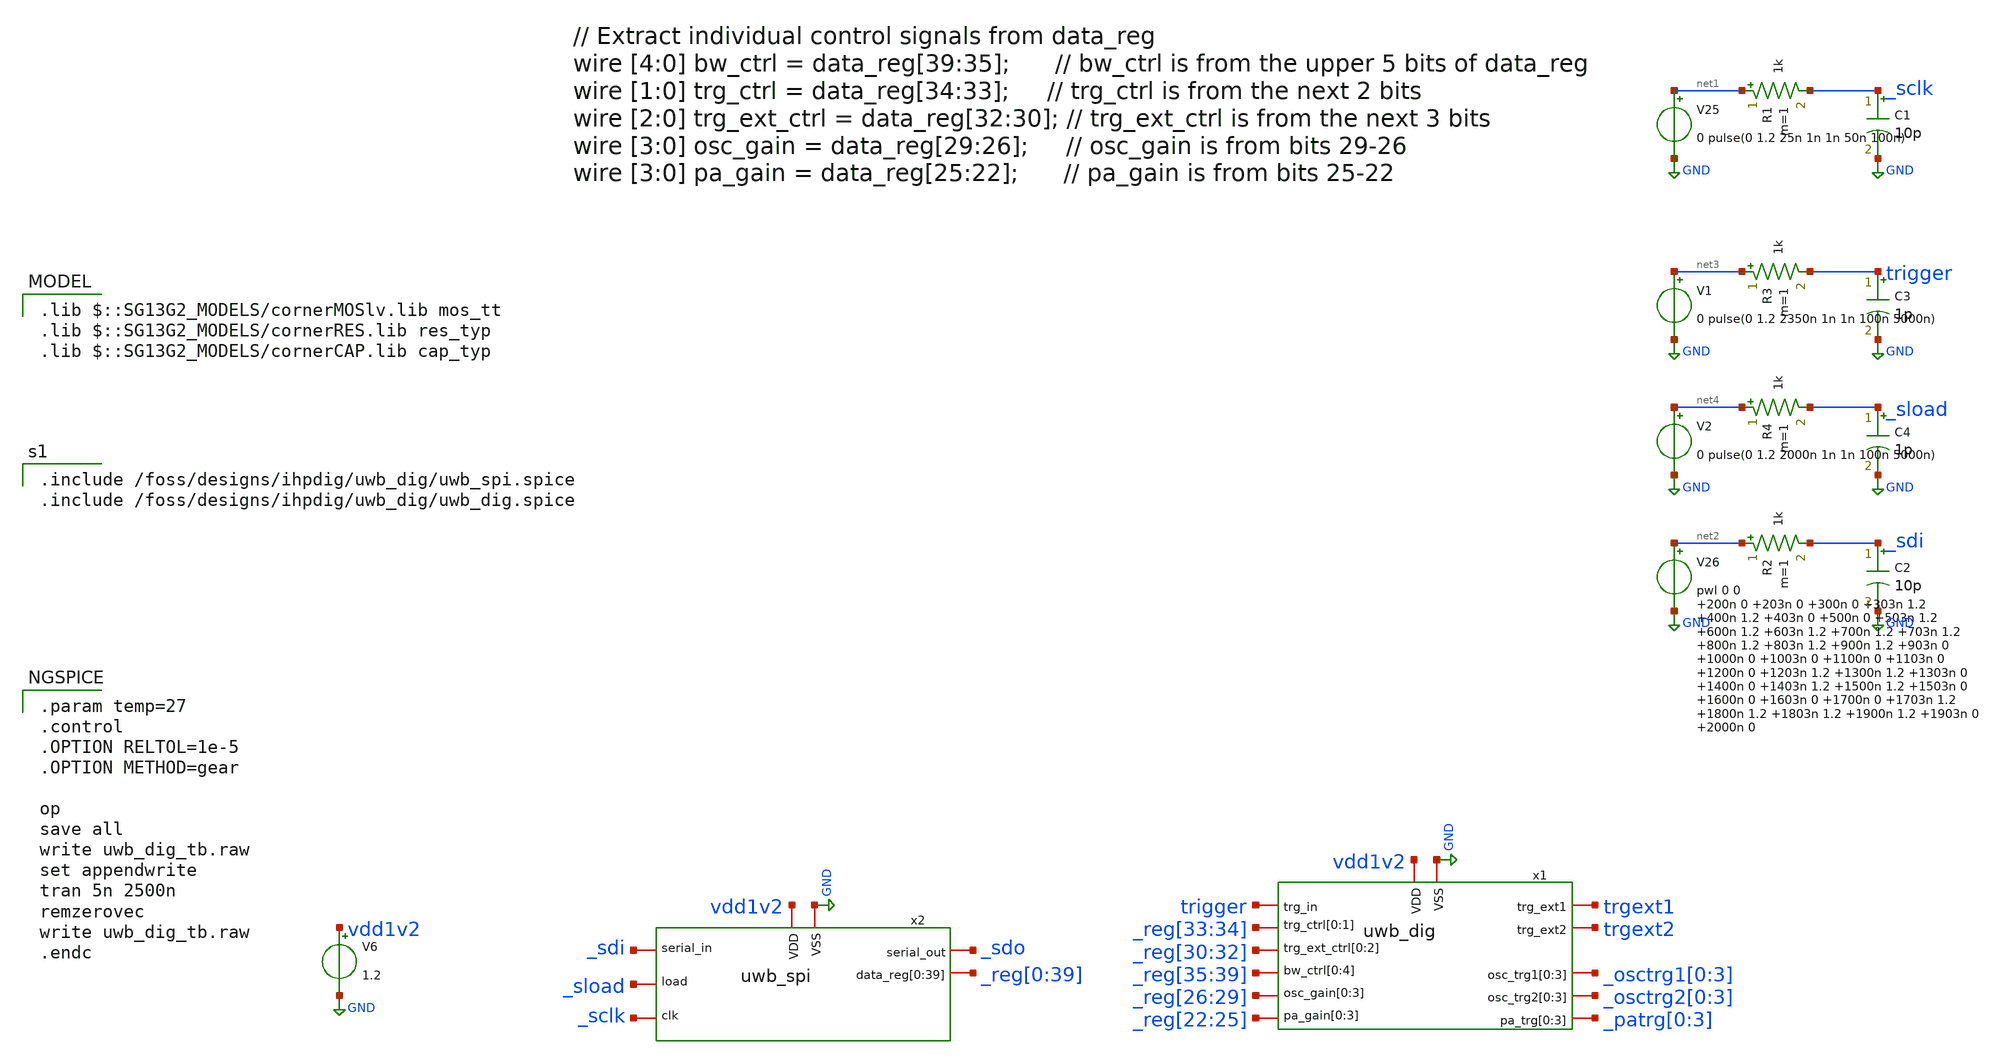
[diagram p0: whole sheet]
** sch_path: JKU_TC2/design_data/xschem/uwb_dig_tb.sch
**.subckt uwb_dig_tb
V6 vdd1v2 GND 1.2
V25 net1 GND 0 pulse(0 1.2 25n 1n 1n 50n 100n)

V26 net2 GND pwl 0 0 200n 0 +203n 0 +300n 0 +303n 1.2 400n 1.2 +403n 0 +500n 0 +503n 1.2 600n 1.2
+ +603n 1.2 +700n 1.2 +703n 1.2 800n 1.2 +803n 1.2 +900n 1.2 +903n 0 1000n 0 +1003n 0 +1100n 0 +1103n 0
+ 1200n 0 +1203n 1.2 +1300n 1.2 +1303n 0 1400n 0 +1403n 1.2 +1500n 1.2 +1503n 0 1600n 0 +1603n 0 +1700n 0
+ +1703n 1.2 1800n 1.2 +1803n 1.2 +1900n 1.2 +1903n 0 2000n 0
V1 net3 GND 0 pulse(0 1.2 2350n 1n 1n 100n 5000n)

C1 _sclk GND 10p m=1
R2 net2 _sdi 1k m=1
C2 _sdi GND 10p m=1
R1 net1 _sclk 1k m=1
R3 net3 trigger 1k m=1
C3 trigger GND 1p m=1
V2 net4 GND 0 pulse(0 1.2 2000n 1n 1n 100n 5000n)

R4 net4 _sload 1k m=1
C4 _sload GND 1p m=1
x1 vdd1v2 GND trgext1 trgext2 trigger _reg[35] _reg[36] _reg[37] _reg[38] _reg[39] _reg[26] _reg[27]
+ _reg[28] _reg[29] _osctrg1[0] _osctrg1[1] _osctrg1[2] _osctrg1[3] _osctrg2[0] _osctrg2[1] _osctrg2[2]
+ _osctrg2[3] _reg[22] _reg[23] _reg[24] _reg[25] _patrg[0] _patrg[1] _patrg[2] _patrg[3] _reg[33] _reg[34]
+ _reg[30] _reg[31] _reg[32] uwb_dig
x2 vdd1v2 GND _sclk _sload _sdi _sdo _reg[0] _reg[1] _reg[2] _reg[3] _reg[4] _reg[5] _reg[6] _reg[7]
+ _reg[8] _reg[9] _reg[10] _reg[11] _reg[12] _reg[13] _reg[14] _reg[15] _reg[16] _reg[17] _reg[18] _reg[19]
+ _reg[20] _reg[21] _reg[22] _reg[23] _reg[24] _reg[25] _reg[26] _reg[27] _reg[28] _reg[29] _reg[30] _reg[31]
+ _reg[32] _reg[33] _reg[34] _reg[35] _reg[36] _reg[37] _reg[38] _reg[39] uwb_spi
**** begin user architecture code

.param temp=27
.control
.OPTION RELTOL=1e-5
.OPTION METHOD=gear

op
save all
write uwb_dig_tb.raw
set appendwrite
tran 5n 2500n
remzerovec
write uwb_dig_tb.raw
.endc



.include /foss/designs/ihpdig/uwb_dig/uwb_spi.spice
.include /foss/designs/ihpdig/uwb_dig/uwb_dig.spice


 .lib $::SG13G2_MODELS/cornerMOSlv.lib mos_tt
.lib $::SG13G2_MODELS/cornerRES.lib res_typ
.lib $::SG13G2_MODELS/cornerCAP.lib cap_typ

**** end user architecture code
**.ends
.GLOBAL GND
.end
